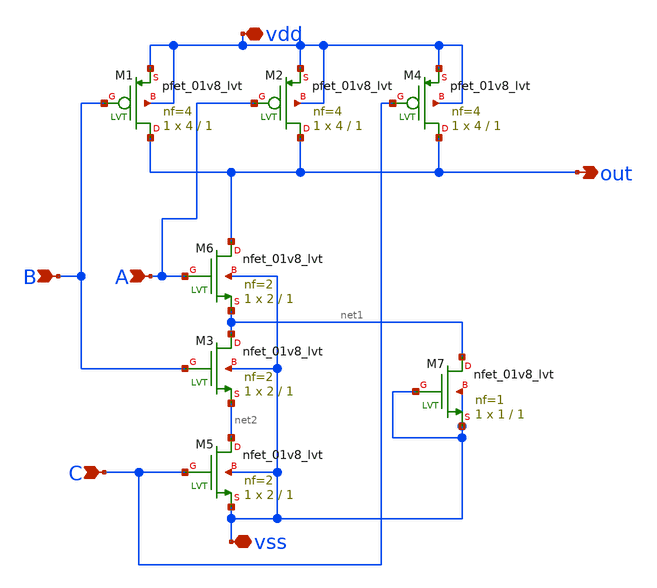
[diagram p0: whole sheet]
** sch_path: BGR_TOP_SKY130A/NAND.sch
**.subckt NAND vdd vss A C B out
*.iopin vdd
*.iopin vss
*.ipin A
*.ipin C
*.ipin B
*.opin out
XM6 out A net1 vss sky130_fd_pr__nfet_01v8_lvt L=1 W=2 nf=2 ad='int((2 + 1)/2) * 2 / 2 * 0.29' as='int((2 + 2)/2) * 2 / 2 * 0.29'
+ pd='2*int((2 + 1)/2) * (2 / 2 + 0.29)' ps='2*int((2 + 2)/2) * (2 / 2 + 0.29)' nrd='0.29 / 2 ' nrs='0.29 / 2 '
+ sa=0 sb=0 sd=0 mult=1 m=1
XM1 out B vdd vdd sky130_fd_pr__pfet_01v8_lvt L=1 W=4 nf=4 ad='int((4 + 1)/2) * 4 / 4 * 0.29' as='int((4 + 2)/2) * 4 / 4 * 0.29'
+ pd='2*int((4 + 1)/2) * (4 / 4 + 0.29)' ps='2*int((4 + 2)/2) * (4 / 4 + 0.29)' nrd='0.29 / 4 ' nrs='0.29 / 4 '
+ sa=0 sb=0 sd=0 mult=1 m=1
XM2 out A vdd vdd sky130_fd_pr__pfet_01v8_lvt L=1 W=4 nf=4 ad='int((4 + 1)/2) * 4 / 4 * 0.29' as='int((4 + 2)/2) * 4 / 4 * 0.29'
+ pd='2*int((4 + 1)/2) * (4 / 4 + 0.29)' ps='2*int((4 + 2)/2) * (4 / 4 + 0.29)' nrd='0.29 / 4 ' nrs='0.29 / 4 '
+ sa=0 sb=0 sd=0 mult=1 m=1
XM3 net1 B net2 vss sky130_fd_pr__nfet_01v8_lvt L=1 W=2 nf=2 ad='int((2 + 1)/2) * 2 / 2 * 0.29' as='int((2 + 2)/2) * 2 / 2 * 0.29'
+ pd='2*int((2 + 1)/2) * (2 / 2 + 0.29)' ps='2*int((2 + 2)/2) * (2 / 2 + 0.29)' nrd='0.29 / 2 ' nrs='0.29 / 2 '
+ sa=0 sb=0 sd=0 mult=1 m=1
XM4 out C vdd vdd sky130_fd_pr__pfet_01v8_lvt L=1 W=4 nf=4 ad='int((4 + 1)/2) * 4 / 4 * 0.29' as='int((4 + 2)/2) * 4 / 4 * 0.29'
+ pd='2*int((4 + 1)/2) * (4 / 4 + 0.29)' ps='2*int((4 + 2)/2) * (4 / 4 + 0.29)' nrd='0.29 / 4 ' nrs='0.29 / 4 '
+ sa=0 sb=0 sd=0 mult=1 m=1
XM5 net2 C vss vss sky130_fd_pr__nfet_01v8_lvt L=1 W=2 nf=2 ad='int((2 + 1)/2) * 2 / 2 * 0.29' as='int((2 + 2)/2) * 2 / 2 * 0.29'
+ pd='2*int((2 + 1)/2) * (2 / 2 + 0.29)' ps='2*int((2 + 2)/2) * (2 / 2 + 0.29)' nrd='0.29 / 2 ' nrs='0.29 / 2 '
+ sa=0 sb=0 sd=0 mult=1 m=1
XM7 net1 vss vss vss sky130_fd_pr__nfet_01v8_lvt L=1 W=1 nf=1 ad='int((1 + 1)/2) * 1 / 1 * 0.29' as='int((1 + 2)/2) * 1 / 1 * 0.29'
+ pd='2*int((1 + 1)/2) * (1 / 1 + 0.29)' ps='2*int((1 + 2)/2) * (1 / 1 + 0.29)' nrd='0.29 / 1 ' nrs='0.29 / 1 '
+ sa=0 sb=0 sd=0 mult=1 m=1
**.ends
.end
